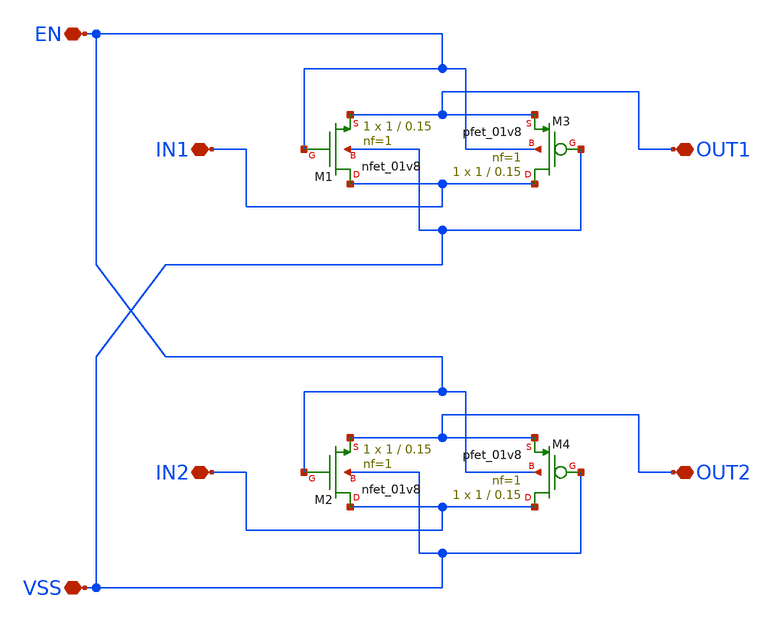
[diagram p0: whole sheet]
** sch_path: npmos_switch2.sch
**.subckt npmos_switch2 EN IN1 OUT1 VSS IN2 OUT2
*.iopin EN
*.iopin IN1
*.iopin OUT1
*.iopin VSS
*.iopin IN2
*.iopin OUT2
XM1 IN1 EN OUT1 VSS sky130_fd_pr__nfet_01v8 L=0.15 W=1 nf=1 ad='int((1 + 1)/2) * 1 / 1 * 0.29' as='int((1 + 2)/2) * 1 / 1 * 0.29'
+ pd='2*int((1 + 1)/2) * (1 / 1 + 0.29)' ps='2*int((1 + 2)/2) * (1 / 1 + 0.29)' nrd='0.29 / 1 ' nrs='0.29 / 1 '
+ sa=0 sb=0 sd=0 mult=1 m=1
XM3 IN1 VSS OUT1 EN sky130_fd_pr__pfet_01v8 L=0.15 W=1 nf=1 ad='int((nf+1)/2) * W/nf * 0.29' as='int((nf+2)/2) * W/nf * 0.29'
+ pd='2*int((nf+1)/2) * (W/nf + 0.29)' ps='2*int((nf+2)/2) * (W/nf + 0.29)' nrd='0.29 / W' nrs='0.29 / W'
+ sa=0 sb=0 sd=0 mult=1 m=1
XM2 IN2 EN OUT2 VSS sky130_fd_pr__nfet_01v8 L=0.15 W=1 nf=1 ad='int((1 + 1)/2) * 1 / 1 * 0.29' as='int((1 + 2)/2) * 1 / 1 * 0.29'
+ pd='2*int((1 + 1)/2) * (1 / 1 + 0.29)' ps='2*int((1 + 2)/2) * (1 / 1 + 0.29)' nrd='0.29 / 1 ' nrs='0.29 / 1 '
+ sa=0 sb=0 sd=0 mult=1 m=1
XM4 IN2 VSS OUT2 EN sky130_fd_pr__pfet_01v8 L=0.15 W=1 nf=1 ad='int((nf+1)/2) * W/nf * 0.29' as='int((nf+2)/2) * W/nf * 0.29'
+ pd='2*int((nf+1)/2) * (W/nf + 0.29)' ps='2*int((nf+2)/2) * (W/nf + 0.29)' nrd='0.29 / W' nrs='0.29 / W'
+ sa=0 sb=0 sd=0 mult=1 m=1
**.ends
.end
